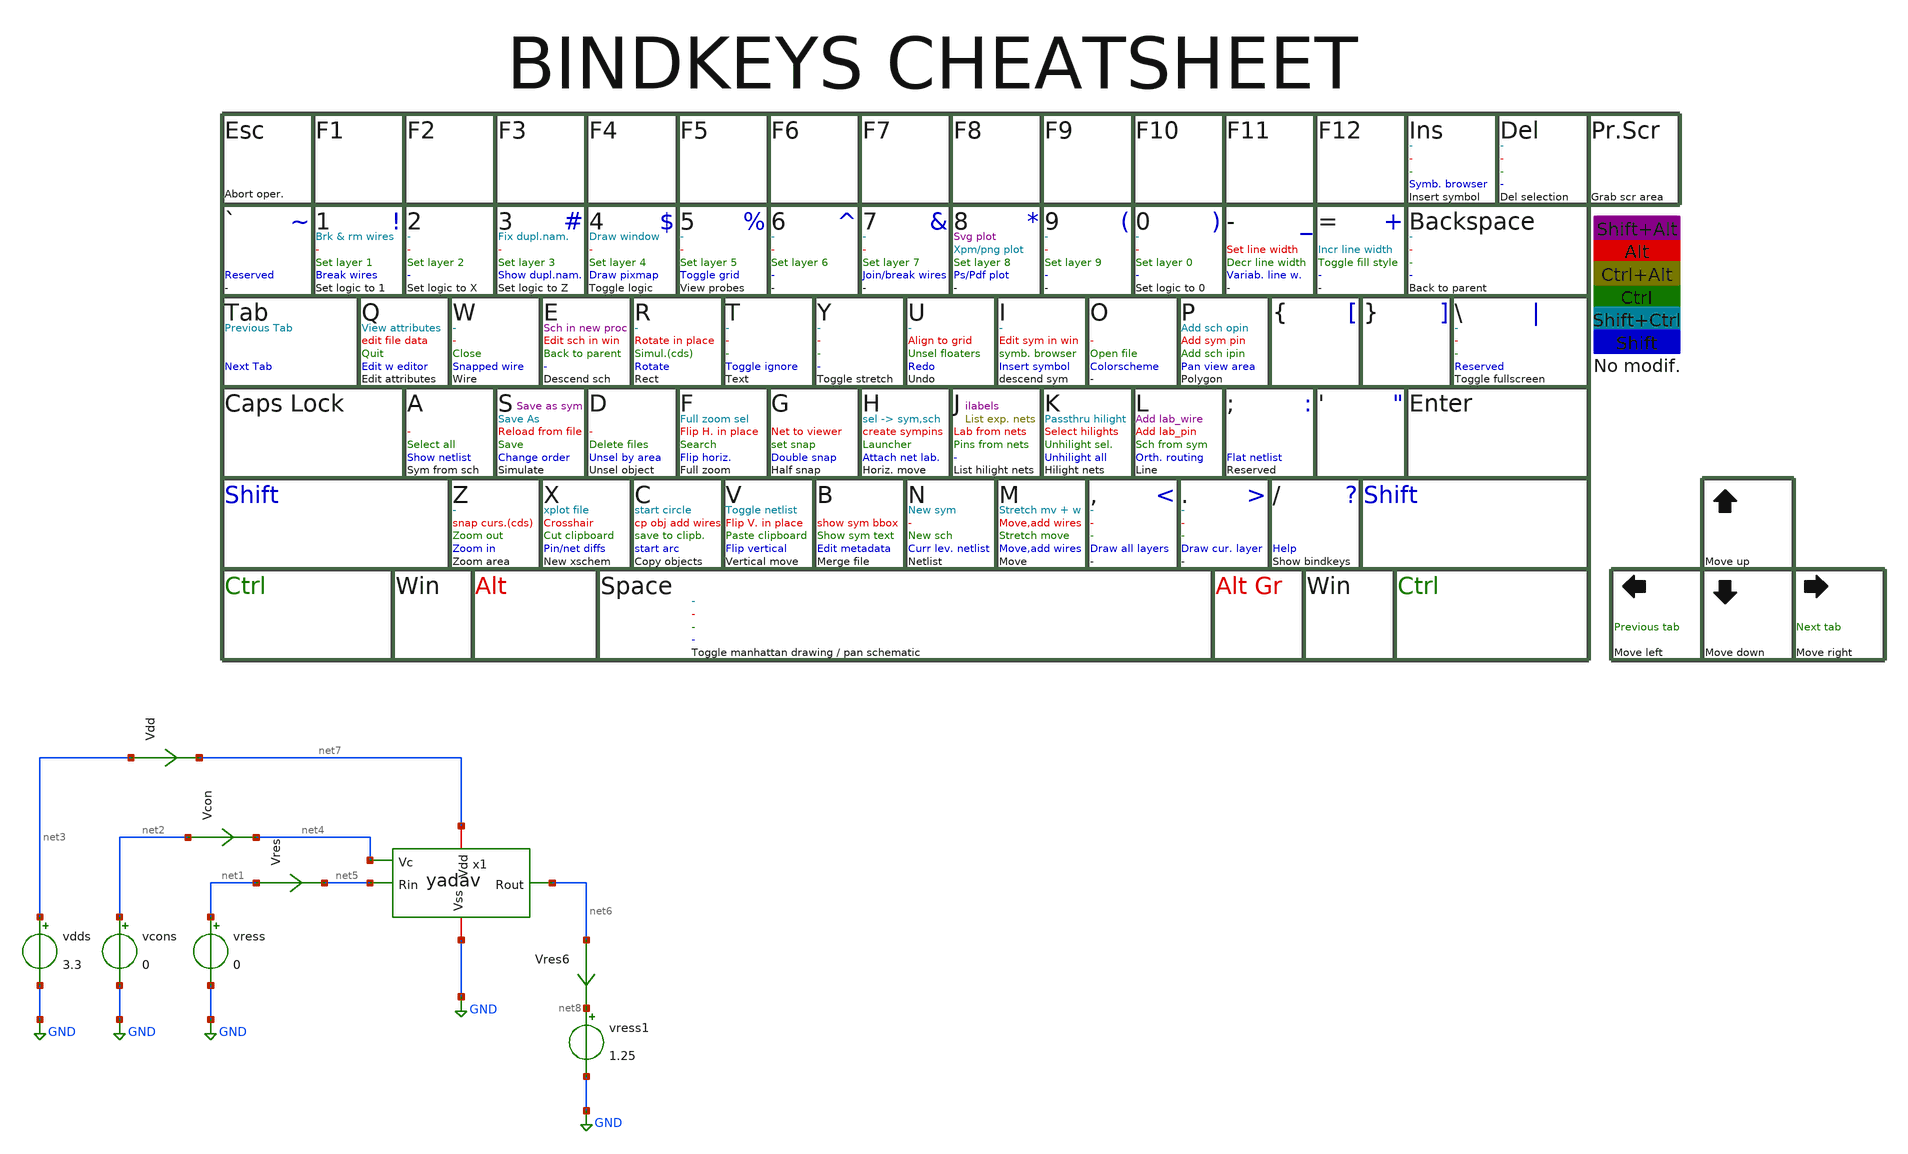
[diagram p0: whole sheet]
** sch_path: macros/heichips26_analog_project/macros/yadav/testbenches/xschem/plm.sch
**.subckt plm
Vres net1 net5 0
.save i(vres)
vress net1 GND 0
vcons net2 GND 0
vdds net3 GND 3.3
Vcon net2 net4 0
.save i(vcon)
Vdd net3 net7 0
.save i(vdd)
vress1 net8 GND 1.25
x1 net7 net5 net6 net4 GND yadav
Vres6 net6 net8 0
.save i(vres6)
**** begin user architecture code


* .include ../../../netlist/pex/inverter_magic_pex_3.spice
.param temp=27
.options savecurrents klu method=gear reltol=1e-3 abstol=1e-15 gmin=1e-15 rshunt=1e10
.control
save all
set appendwrite

* DC Sweep
* dc vcon 1 1.5 1m
* remzerovec

* plot v(vres)/i(Vres)
*plot v(VStage1)
*plot v(VStage2)



let vcc = 0.4
repeat 5
  alter vcons $&vcc

  * DC Sweep
  dc vress 0.3 3.3 1m
  remzerovec
  let vcc = vcc + 0.15
end
set appendwrite

*plot dc1.v(V1)/(dc1.i(Vres)) dc2.v(V1)/(dc2.i(Vres)) dc3.v(V1)/(dc3.i(Vres))
*+ dc4.v(V1)/(dc4.i(Vres)) dc5.v(V1)/(dc5.i(Vres))

*plot dc1.v(V1)/(dc1.i(Vres6)) dc2.v(V1)/(dc2.i(Vres6)) dc3.v(V1)/(dc3.i(Vres6))
*+ dc4.v(V1)/(dc4.i(Vres6)) dc5.v(V1)/(dc5.i(Vres6))

plot (dc1.i(Vres)) (dc2.i(Vres)) (dc3.i(Vres)) (dc4.i(Vres)) (dc5.i(Vres))

plot (dc1.i(Vres6)) (dc2.i(Vres6)) (dc3.i(Vres6)) (dc4.i(Vres6))  (dc5.i(Vres6))


* Write Data
unset appendwrite
set wr_vecnames
set wr_singlescale

*quit
.endc



.lib cornerMOSlv.lib mos_tt
.lib cornerMOShv.lib mos_tt
.lib cornerRES.lib res_typ
.lib cornerDIO.lib dio_tt

**** end user architecture code
**.ends

* expanding   symbol:  yadav.sym # of pins=5
** sym_path: macros/heichips26_analog_project/macros/yadav/schematic/xschem/yadav.sym
** sch_path: macros/heichips26_analog_project/macros/yadav/schematic/xschem/yadav.sch
.subckt yadav Vdd Rin Rout Vc Vss
*.ipin Vc
*.iopin Vss
*.iopin Vdd
*.ipin Rin
*.opin Rout
XM3 Vdd Rin net2 Vss sg13_hv_nmos w=0.72u l=4.14u ng=2 m=1 mm_ok=1
XM13 net1 net1 Vdd Vdd sg13_hv_pmos w=18.5u l=2.16u ng=2 m=1 mm_ok=1
XM1 net4 Rin net3 Vss sg13_hv_nmos w=0.72u l=4.14u ng=2 m=1 mm_ok=1
XM5 net1 net2 net3 Vss sg13_hv_nmos w=0.72u l=4.14u ng=2 m=1 mm_ok=1
XM2 net1 Rout net3 Vss sg13_hv_nmos w=0.72u l=4.14u ng=2 m=1 mm_ok=1
XM16 net4 net4 Vdd Vdd sg13_hv_pmos w=18.5u l=2.16u ng=2 m=1 mm_ok=1
XM7 net2 Vc Vss Vss sg13_hv_nmos w=0.72u l=4.14u ng=2 m=1 mm_ok=1
XM6 net4 net7 net3 Vss sg13_hv_nmos w=0.72u l=4.14u ng=2 m=1 mm_ok=1
XM14 net5 net1 Vdd Vdd sg13_hv_pmos w=18.5u l=2.16u ng=2 m=1 mm_ok=1
XM8 net7 Vc Vss Vss sg13_hv_nmos w=0.72u l=4.14u ng=2 m=1 mm_ok=1
XM4 Vdd Rout net7 Vss sg13_hv_nmos w=0.72u l=4.14u ng=2 m=1 mm_ok=1
XM9 net5 net5 Vss Vss sg13_hv_nmos w=0.72u l=2.16u ng=2 m=1 mm_ok=1
XM10 Rout net5 Vss Vss sg13_hv_nmos w=0.72u l=2.16u ng=2 m=1 mm_ok=1
XM17 Rout net4 Vdd Vdd sg13_hv_pmos w=18.5u l=2.16u ng=2 m=1 mm_ok=1
XM18 net6 net4 Vdd Vdd sg13_hv_pmos w=18.5u l=2.16u ng=2 m=1 mm_ok=1
XM11 net6 net6 Vss Vss sg13_hv_nmos w=0.72u l=2.16u ng=2 m=1 mm_ok=1
XM12 Rin net6 Vss Vss sg13_hv_nmos w=0.72u l=2.16u ng=2 m=1 mm_ok=1
XM15 Rin net1 Vdd Vdd sg13_hv_pmos w=18.5u l=2.16u ng=2 m=1 mm_ok=1
I0 net3 Vss 60u
.ends

.GLOBAL GND
.end
